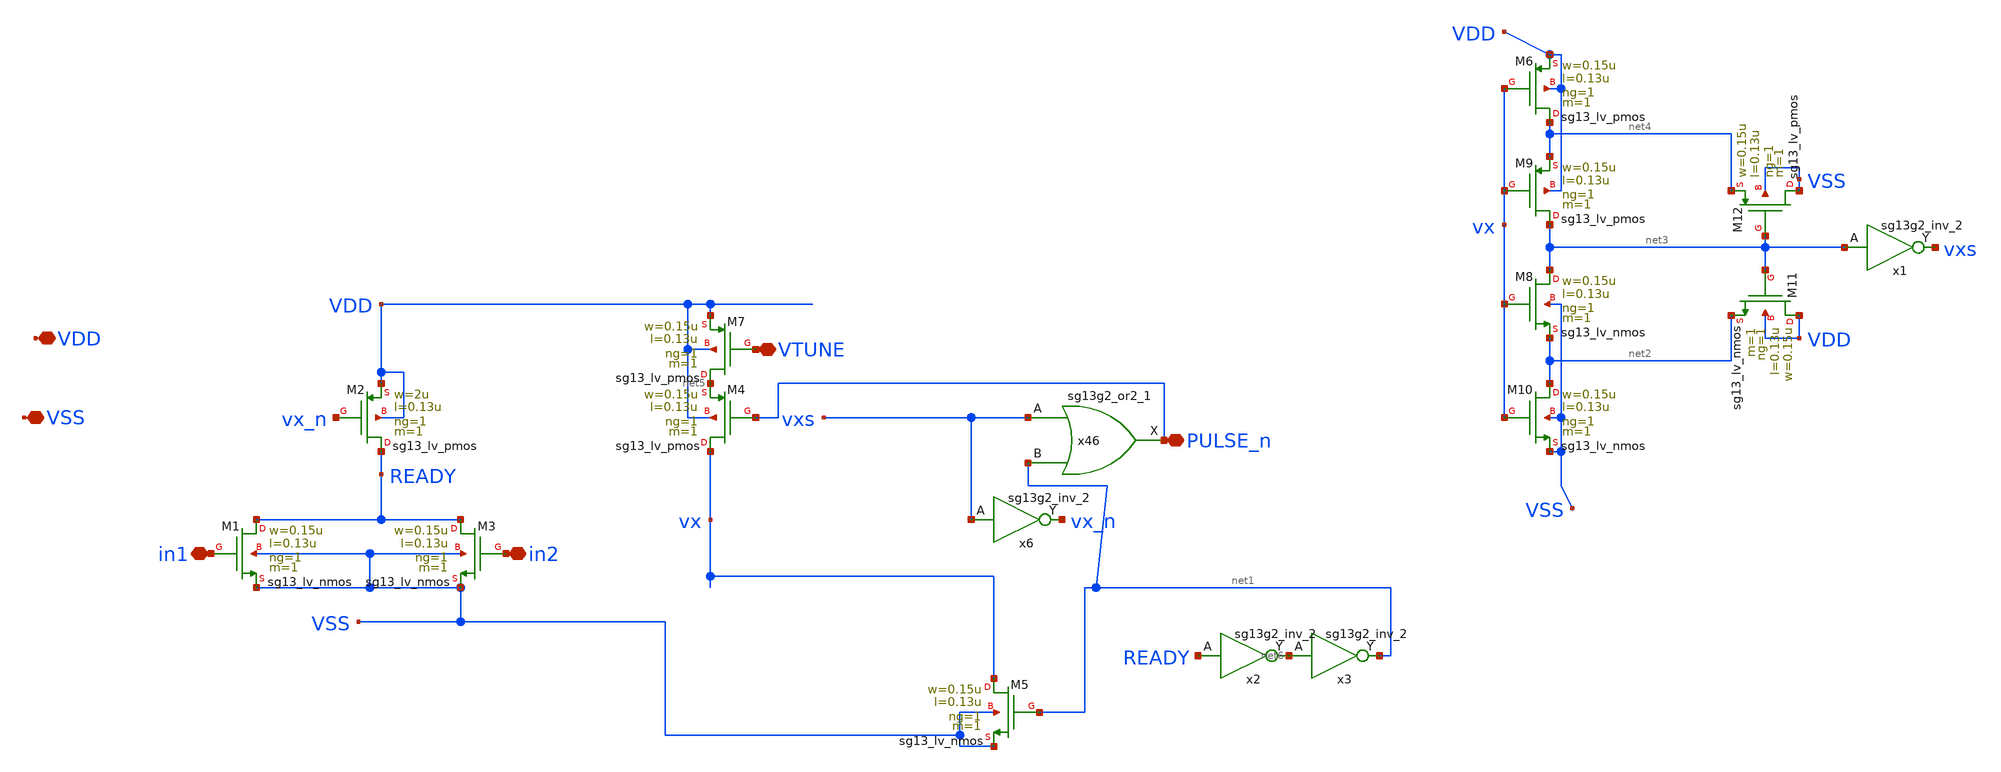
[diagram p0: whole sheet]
** sch_path: xschem/comparator/pulse_gen/pgen.sch
* IHP-GmbH/IHP-Open-PDK/ihp-sg13g2/libs.tech/xschem/sg13g2_stdcells/sg13g2_inv_2.sch:
* Copyright 2023 IHP PDK Authors
* Licensed under the Apache License, Version 2.0 (the "License");
**.subckt pgen VDD in2 in1 VSS VTUNE PULSE_n
*.iopin VDD
*.iopin in2
*.iopin in1
*.iopin VSS
*.iopin VTUNE
*.iopin PULSE_n
XM1 READY in1 VSS VSS sg13_lv_nmos w=0.15u l=0.13u ng=1 m=1 mm_ok=1
XM2 READY vx_n VDD VDD sg13_lv_pmos w=2u l=0.13u ng=1 m=1 mm_ok=1
XM4 vx PULSE_n net5 VDD sg13_lv_pmos w=0.15u l=0.13u ng=1 m=1 mm_ok=1
x46 PULSE_n vxs net1 VDD VSS sg13g2_or2_1
x6 vx_n vxs VDD VSS sg13g2_inv_2
XM3 READY in2 VSS VSS sg13_lv_nmos w=0.15u l=0.13u ng=1 m=1 mm_ok=1
XM5 vx net1 VSS VSS sg13_lv_nmos w=0.15u l=0.13u ng=1 m=1 mm_ok=1
XM7 net5 VTUNE VDD VDD sg13_lv_pmos w=0.15u l=0.13u ng=1 m=1 mm_ok=1
XM6 net4 vx VDD VDD sg13_lv_pmos w=0.15u l=0.13u ng=1 m=1 mm_ok=1
XM8 net3 vx net2 VSS sg13_lv_nmos w=0.15u l=0.13u ng=1 m=1 mm_ok=1
XM9 net3 vx net4 VDD sg13_lv_pmos w=0.15u l=0.13u ng=1 m=1 mm_ok=1
XM10 net2 vx VSS VSS sg13_lv_nmos w=0.15u l=0.13u ng=1 m=1 mm_ok=1
XM11 VDD net3 net2 VDD sg13_lv_nmos w=0.15u l=0.13u ng=1 m=1 mm_ok=1
XM12 VSS net3 net4 VSS sg13_lv_pmos w=0.15u l=0.13u ng=1 m=1 mm_ok=1
x1 vxs net3 VDD VSS sg13g2_inv_2
x2 net6 READY VDD VSS sg13g2_inv_2
x3 net1 net6 VDD VSS sg13g2_inv_2
**.ends

* expanding   symbol:  sg13g2_stdcells/sg13g2_or2_1.sym # of pins=3
** sym_path: sg13g2_stdcells/sg13g2_or2_1.sym
** sch_path: sg13g2_stdcells/sg13g2_or2_1.sch
.subckt sg13g2_or2_1 X A B VDD VSS
*.opin X
*.ipin B
*.ipin A
*.iopin VDD
*.iopin VSS
XM1 net1 B VSS VSS sg13_lv_nmos w=550.00n l=130.00n ng=1 m=1 mm_ok=1
XM2 net1 A VSS VSS sg13_lv_nmos w=550.00n l=130.00n ng=1 m=1 mm_ok=1
XM3 X net1 VSS VSS sg13_lv_nmos w=740.00n l=130.00n ng=1 m=1 mm_ok=1
XM4 net2 A VDD VDD sg13_lv_pmos w=840.00n l=130.00n ng=1 m=1 mm_ok=1
XM5 net1 B net2 VDD sg13_lv_pmos w=840.00n l=130.00n ng=1 m=1 mm_ok=1
XM6 X net1 VDD VDD sg13_lv_pmos w=1.12u l=130.00n ng=1 m=1 mm_ok=1
.ends


* expanding   symbol:  sg13g2_stdcells/sg13g2_inv_2.sym # of pins=2
** sym_path: sg13g2_stdcells/sg13g2_inv_2.sym
** sch_path: sg13g2_stdcells/sg13g2_inv_2.sch
.subckt sg13g2_inv_2 Y A VDD VSS
*.opin Y
*.ipin A
*.iopin VDD
*.iopin VSS
XM1 Y A VSS VSS sg13_lv_nmos w=1.48u l=130.00n ng=2 m=1 mm_ok=1
XM2 Y A VDD VDD sg13_lv_pmos w=2.24u l=130.00n ng=2 m=1 mm_ok=1
.ends

.end
